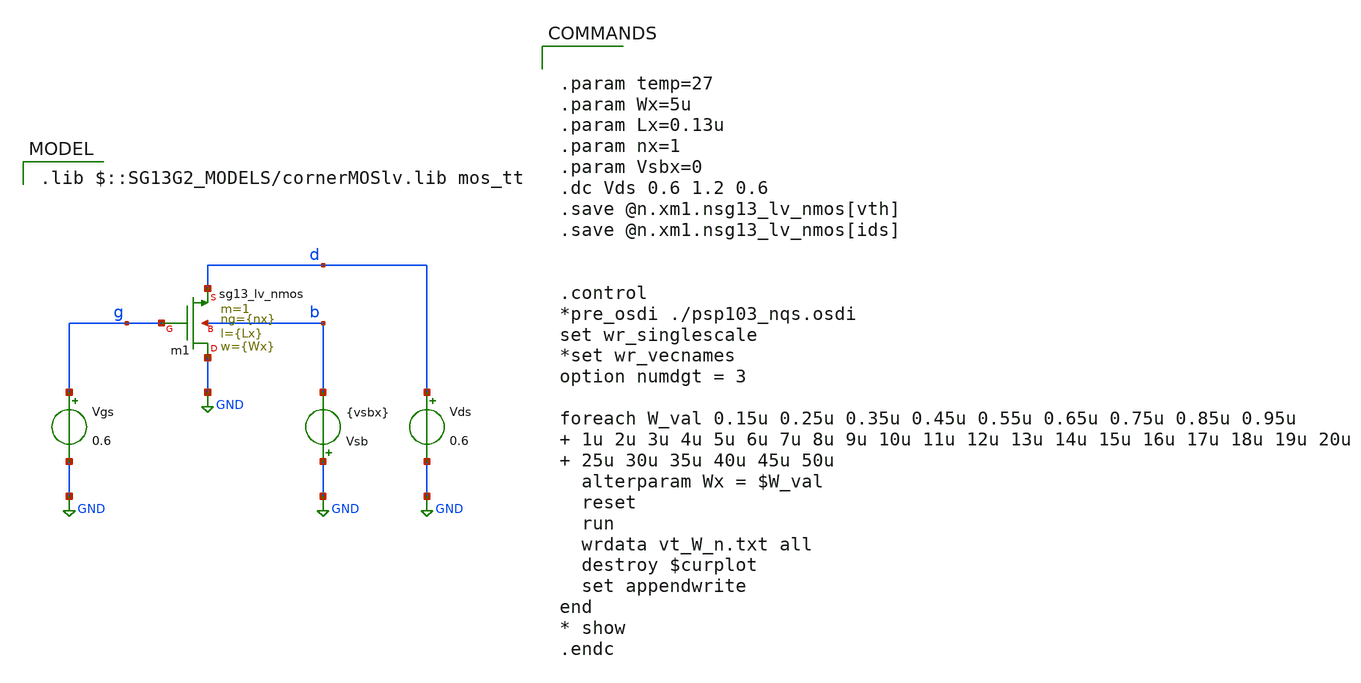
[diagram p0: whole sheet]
** sch_path: 01_technology/01_vt_W/src/vt_W_n.sch
**.subckt vt_W_n
Xm1 GND g d b sg13_lv_nmos w={Wx} l={Lx} ng={nx} m=1 mm_ok=1
Vgs g GND 0.6
Vds d GND 0.6
Vsb GND b {vsbx}
**** begin user architecture code
 .lib $::SG13G2_MODELS/cornerMOSlv.lib mos_tt



.param temp=27
.param Wx=5u
.param Lx=0.13u
.param nx=1
.param Vsbx=0
.dc Vds 0.6 1.2 0.6
.save @n.xm1.nsg13_lv_nmos[vth]
.save @n.xm1.nsg13_lv_nmos[ids]


.control
*pre_osdi ./psp103_nqs.osdi
set wr_singlescale
*set wr_vecnames
option numdgt = 3

foreach W_val 0.15u 0.25u 0.35u 0.45u 0.55u 0.65u 0.75u 0.85u 0.95u  1u 2u 3u 4u 5u 6u 7u 8u 9u 10u
+ 11u 12u 13u 14u 15u 16u 17u 18u 19u 20u  25u 30u 35u 40u 45u 50u
  alterparam Wx = $W_val
  reset
  run
  wrdata vt_W_n.txt all
  destroy $curplot
  set appendwrite
end
* show
.endc


**** end user architecture code
**.ends
.GLOBAL GND
.end
